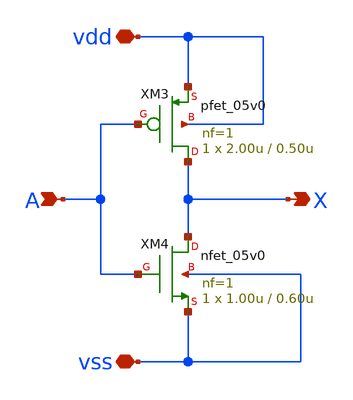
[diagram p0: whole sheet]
** sch_path: xschem/hv_inv_1.sch
**.subckt hv_inv_1 A vdd vss X
*.ipin A
*.iopin vdd
*.iopin vss
*.opin X
XM3 X A vdd vdd pfet_05v0 L=0.50u W=2.00u nf=1 ad='int((nf+1)/2) * W/nf * 0.18u' as='int((nf+2)/2) * W/nf * 0.18u'
+ pd='2*int((nf+1)/2) * (W/nf + 0.18u)' ps='2*int((nf+2)/2) * (W/nf + 0.18u)' nrd='0.18u / W' nrs='0.18u / W'
+ sa=0 sb=0 sd=0 m=1 par=1
XM4 X A vss vss nfet_05v0 L=0.60u W=1.00u nf=1 ad='int((nf+1)/2) * W/nf * 0.18u' as='int((nf+2)/2) * W/nf * 0.18u'
+ pd='2*int((nf+1)/2) * (W/nf + 0.18u)' ps='2*int((nf+2)/2) * (W/nf + 0.18u)' nrd='0.18u / W' nrs='0.18u / W'
+ sa=0 sb=0 sd=0 m=1
**.ends
.end
